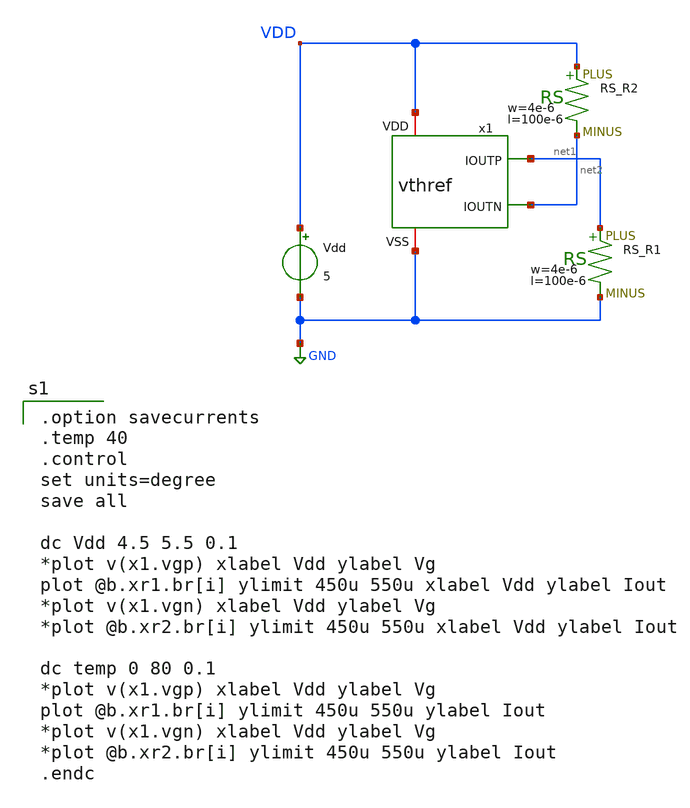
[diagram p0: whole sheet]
** sch_path: Vol.2/files/03/xschem/test_vthref_dc.sch
**.subckt test_vthref_dc
Vdd VDD GND 5
XR1 net1 GND F_RS w=4e-6 R=1 l=100e-6 tc1=0 tc2=0
x1 VDD net1 net2 GND vthref
XR2 VDD net2 F_RS w=4e-6 R=1 l=100e-6 tc1=0 tc2=0
**** begin user architecture code
 .include $::LIB/../ip62_models

.option savecurrents
.temp 40
.control
set units=degree
save all

dc Vdd 4.5 5.5 0.1
*plot v(x1.vgp) xlabel Vdd ylabel Vg
plot @b.xr1.br[i] ylimit 450u 550u xlabel Vdd ylabel Iout
*plot v(x1.vgn) xlabel Vdd ylabel Vg
*plot @b.xr2.br[i] ylimit 450u 550u xlabel Vdd ylabel Iout

dc temp 0 80 0.1
*plot v(x1.vgp) xlabel Vdd ylabel Vg
plot @b.xr1.br[i] ylimit 450u 550u ylabel Iout
*plot v(x1.vgn) xlabel Vdd ylabel Vg
*plot @b.xr2.br[i] ylimit 450u 550u ylabel Iout
.endc

**** end user architecture code
**.ends
.GLOBAL GND
.end
